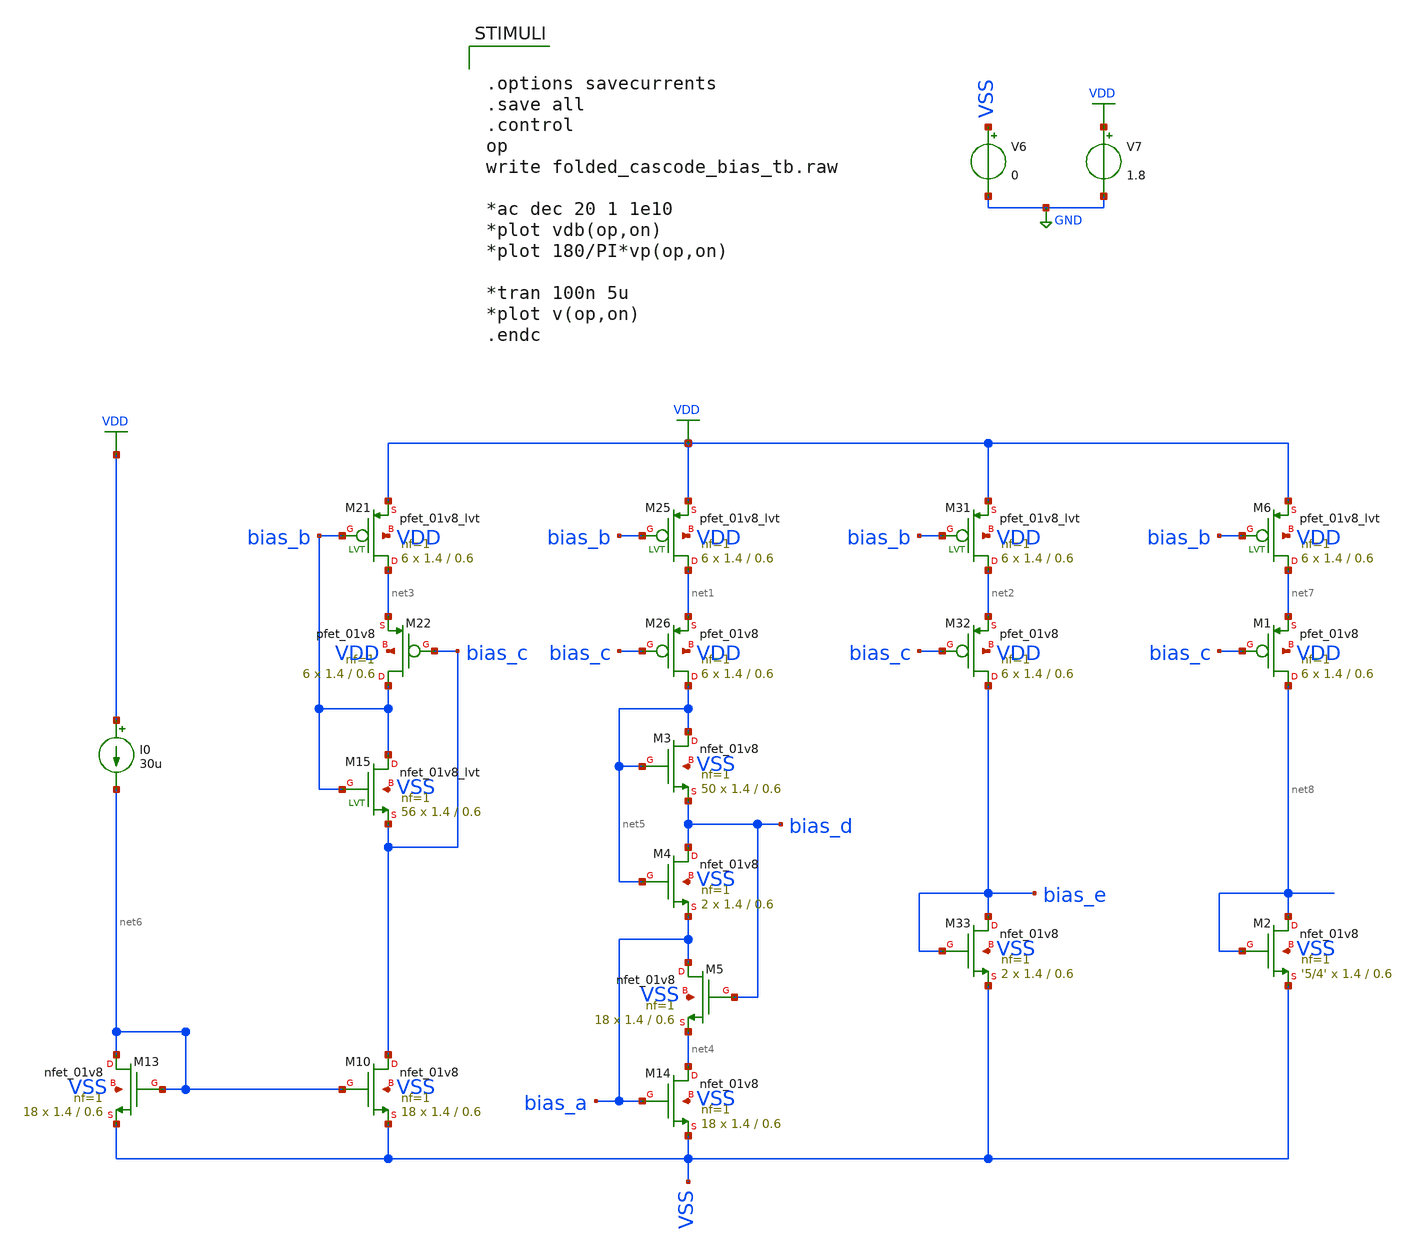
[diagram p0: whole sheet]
** sch_path: verification/schematic/folded_cascode_bias_tb.sch
**.subckt folded_cascode_bias_tb
V6 VSS GND 0
V7 VDD GND 1.8
XM22 bias_b bias_c net3 VDD sky130_fd_pr__pfet_01v8 L=0.6 W=1.4 nf=1 ad='int((nf+1)/2) * W/nf * 0.29'
+ as='int((nf+2)/2) * W/nf * 0.29' pd='2*int((nf+1)/2) * (W/nf + 0.29)' ps='2*int((nf+2)/2) * (W/nf + 0.29)'
+ nrd='0.29 / W' nrs='0.29 / W' sa=0 sb=0 sd=0 mult=6 m=6
XM26 net5 bias_c net1 VDD sky130_fd_pr__pfet_01v8 L=0.6 W=1.4 nf=1 ad='int((nf+1)/2) * W/nf * 0.29' as='int((nf+2)/2) * W/nf * 0.29'
+ pd='2*int((nf+1)/2) * (W/nf + 0.29)' ps='2*int((nf+2)/2) * (W/nf + 0.29)' nrd='0.29 / W' nrs='0.29 / W'
+ sa=0 sb=0 sd=0 mult=6 m=6
XM32 bias_e bias_c net2 VDD sky130_fd_pr__pfet_01v8 L=0.6 W=1.4 nf=1 ad='int((nf+1)/2) * W/nf * 0.29'
+ as='int((nf+2)/2) * W/nf * 0.29' pd='2*int((nf+1)/2) * (W/nf + 0.29)' ps='2*int((nf+2)/2) * (W/nf + 0.29)'
+ nrd='0.29 / W' nrs='0.29 / W' sa=0 sb=0 sd=0 mult=6 m=6
XM33 bias_e bias_e VSS VSS sky130_fd_pr__nfet_01v8 L=0.6 W=1.4 nf=1 ad='int((nf+1)/2) * W/nf * 0.29'
+ as='int((nf+2)/2) * W/nf * 0.29' pd='2*int((nf+1)/2) * (W/nf + 0.29)' ps='2*int((nf+2)/2) * (W/nf + 0.29)'
+ nrd='0.29 / W' nrs='0.29 / W' sa=0 sb=0 sd=0 mult=2 m=2
XM21 net3 bias_b VDD VDD sky130_fd_pr__pfet_01v8_lvt L=0.6 W=1.4 nf=1 ad='int((nf+1)/2) * W/nf * 0.29'
+ as='int((nf+2)/2) * W/nf * 0.29' pd='2*int((nf+1)/2) * (W/nf + 0.29)' ps='2*int((nf+2)/2) * (W/nf + 0.29)'
+ nrd='0.29 / W' nrs='0.29 / W' sa=0 sb=0 sd=0 mult=6 m=6
XM25 net1 bias_b VDD VDD sky130_fd_pr__pfet_01v8_lvt L=0.6 W=1.4 nf=1 ad='int((nf+1)/2) * W/nf * 0.29'
+ as='int((nf+2)/2) * W/nf * 0.29' pd='2*int((nf+1)/2) * (W/nf + 0.29)' ps='2*int((nf+2)/2) * (W/nf + 0.29)'
+ nrd='0.29 / W' nrs='0.29 / W' sa=0 sb=0 sd=0 mult=6 m=6
XM31 net2 bias_b VDD VDD sky130_fd_pr__pfet_01v8_lvt L=0.6 W=1.4 nf=1 ad='int((nf+1)/2) * W/nf * 0.29'
+ as='int((nf+2)/2) * W/nf * 0.29' pd='2*int((nf+1)/2) * (W/nf + 0.29)' ps='2*int((nf+2)/2) * (W/nf + 0.29)'
+ nrd='0.29 / W' nrs='0.29 / W' sa=0 sb=0 sd=0 mult=6 m=6
XM3 net5 net5 bias_d VSS sky130_fd_pr__nfet_01v8 L=0.6 W=1.4 nf=1 ad='int((nf+1)/2) * W/nf * 0.29' as='int((nf+2)/2) * W/nf * 0.29'
+ pd='2*int((nf+1)/2) * (W/nf + 0.29)' ps='2*int((nf+2)/2) * (W/nf + 0.29)' nrd='0.29 / W' nrs='0.29 / W'
+ sa=0 sb=0 sd=0 mult=50 m=50
XM4 bias_d net5 bias_a VSS sky130_fd_pr__nfet_01v8 L=0.6 W=1.4 nf=1 ad='int((nf+1)/2) * W/nf * 0.29'
+ as='int((nf+2)/2) * W/nf * 0.29' pd='2*int((nf+1)/2) * (W/nf + 0.29)' ps='2*int((nf+2)/2) * (W/nf + 0.29)'
+ nrd='0.29 / W' nrs='0.29 / W' sa=0 sb=0 sd=0 mult=2 m=2
XM5 bias_a bias_d net4 VSS sky130_fd_pr__nfet_01v8 L=0.6 W=1.4 nf=1 ad='int((nf+1)/2) * W/nf * 0.29'
+ as='int((nf+2)/2) * W/nf * 0.29' pd='2*int((nf+1)/2) * (W/nf + 0.29)' ps='2*int((nf+2)/2) * (W/nf + 0.29)'
+ nrd='0.29 / W' nrs='0.29 / W' sa=0 sb=0 sd=0 mult=18 m=18
XM14 net4 bias_a VSS VSS sky130_fd_pr__nfet_01v8 L=0.6 W=1.4 nf=1 ad='int((nf+1)/2) * W/nf * 0.29' as='int((nf+2)/2) * W/nf * 0.29'
+ pd='2*int((nf+1)/2) * (W/nf + 0.29)' ps='2*int((nf+2)/2) * (W/nf + 0.29)' nrd='0.29 / W' nrs='0.29 / W'
+ sa=0 sb=0 sd=0 mult=18 m=18
XM15 bias_b bias_b bias_c VSS sky130_fd_pr__nfet_01v8_lvt L=0.6 W=1.4 nf=1 ad='int((nf+1)/2) * W/nf * 0.29'
+ as='int((nf+2)/2) * W/nf * 0.29' pd='2*int((nf+1)/2) * (W/nf + 0.29)' ps='2*int((nf+2)/2) * (W/nf + 0.29)'
+ nrd='0.29 / W' nrs='0.29 / W' sa=0 sb=0 sd=0 mult=56 m=56
XM10 bias_c net6 VSS VSS sky130_fd_pr__nfet_01v8 L=0.6 W=1.4 nf=1 ad='int((nf+1)/2) * W/nf * 0.29' as='int((nf+2)/2) * W/nf * 0.29'
+ pd='2*int((nf+1)/2) * (W/nf + 0.29)' ps='2*int((nf+2)/2) * (W/nf + 0.29)' nrd='0.29 / W' nrs='0.29 / W'
+ sa=0 sb=0 sd=0 mult=18 m=18
XM13 net6 net6 VSS VSS sky130_fd_pr__nfet_01v8 L=0.6 W=1.4 nf=1 ad='int((nf+1)/2) * W/nf * 0.29' as='int((nf+2)/2) * W/nf * 0.29'
+ pd='2*int((nf+1)/2) * (W/nf + 0.29)' ps='2*int((nf+2)/2) * (W/nf + 0.29)' nrd='0.29 / W' nrs='0.29 / W'
+ sa=0 sb=0 sd=0 mult=18 m=18
I0 VDD net6 30u
XM1 net8 bias_c net7 VDD sky130_fd_pr__pfet_01v8 L=0.6 W=1.4 nf=1 ad='int((nf+1)/2) * W/nf * 0.29' as='int((nf+2)/2) * W/nf * 0.29'
+ pd='2*int((nf+1)/2) * (W/nf + 0.29)' ps='2*int((nf+2)/2) * (W/nf + 0.29)' nrd='0.29 / W' nrs='0.29 / W'
+ sa=0 sb=0 sd=0 mult=6 m=6
XM2 net8 net8 VSS VSS sky130_fd_pr__nfet_01v8 L=0.6 W=1.4 nf=1 ad='int((nf+1)/2) * W/nf * 0.29' as='int((nf+2)/2) * W/nf * 0.29'
+ pd='2*int((nf+1)/2) * (W/nf + 0.29)' ps='2*int((nf+2)/2) * (W/nf + 0.29)' nrd='0.29 / W' nrs='0.29 / W'
+ sa=0 sb=0 sd=0 mult='5/4' m='5/4'
XM6 net7 bias_b VDD VDD sky130_fd_pr__pfet_01v8_lvt L=0.6 W=1.4 nf=1 ad='int((nf+1)/2) * W/nf * 0.29'
+ as='int((nf+2)/2) * W/nf * 0.29' pd='2*int((nf+1)/2) * (W/nf + 0.29)' ps='2*int((nf+2)/2) * (W/nf + 0.29)'
+ nrd='0.29 / W' nrs='0.29 / W' sa=0 sb=0 sd=0 mult=6 m=6
**** begin user architecture code

** opencircuitdesign pdks install
.lib /farmshare/home/classes/ee/372/PDKs/open_pdks_1.0.310/sky130/sky130A/libs.tech/ngspice/sky130.lib.spice tt



.options savecurrents
.save all
.control
op
write folded_cascode_bias_tb.raw

*ac dec 20 1 1e10
*plot vdb(op,on)
*plot 180/PI*vp(op,on)

*tran 100n 5u
*plot v(op,on)
.endc


**** end user architecture code
**.ends
.GLOBAL VDD
.GLOBAL GND
.end
